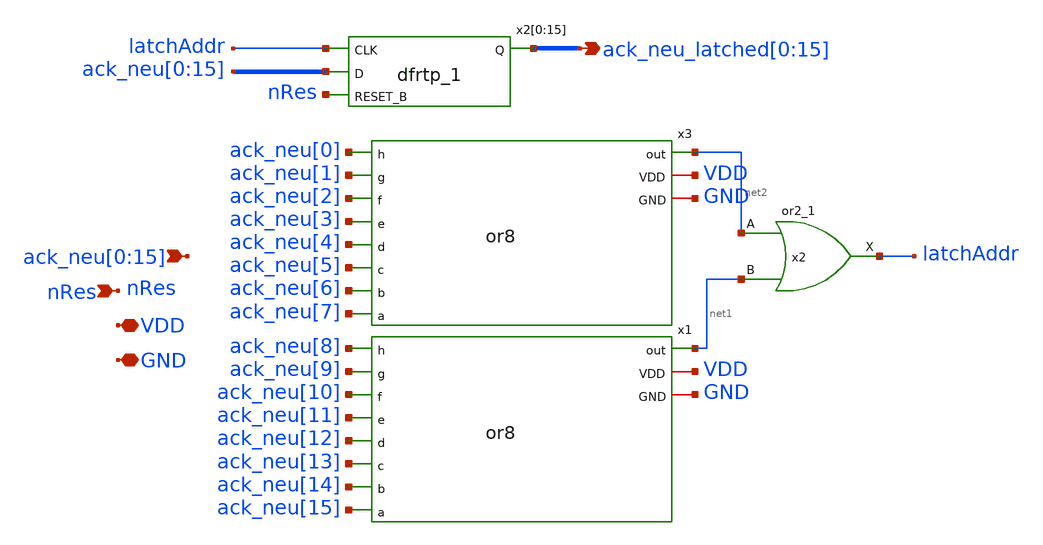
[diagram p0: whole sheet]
** sch_path: design/xschem/output_latch_16_neu.sch
**.subckt output_latch_16_neu
*+ ack_neu[0],ack_neu[1],ack_neu[2],ack_neu[3],ack_neu[4],ack_neu[5],ack_neu[6],ack_neu[7],ack_neu[8],ack_neu[9],ack_neu[10],ack_neu[11],ack_neu[12],ack_neu[13],ack_neu[14],ack_neu[15] nRes
*+ ack_neu_latched[0],ack_neu_latched[1],ack_neu_latched[2],ack_neu_latched[3],ack_neu_latched[4],ack_neu_latched[5],ack_neu_latched[6],ack_neu_latched[7],ack_neu_latched[8],ack_neu_latched[9],ack_neu_latched[10],ack_neu_latched[11],ack_neu_latched[12],ack_neu_latched[13],ack_neu_latched[14],ack_neu_latched[15] VDD GND
*.ipin
*+ ack_neu[0],ack_neu[1],ack_neu[2],ack_neu[3],ack_neu[4],ack_neu[5],ack_neu[6],ack_neu[7],ack_neu[8],ack_neu[9],ack_neu[10],ack_neu[11],ack_neu[12],ack_neu[13],ack_neu[14],ack_neu[15]
*.ipin nRes
*.opin
*+ ack_neu_latched[0],ack_neu_latched[1],ack_neu_latched[2],ack_neu_latched[3],ack_neu_latched[4],ack_neu_latched[5],ack_neu_latched[6],ack_neu_latched[7],ack_neu_latched[8],ack_neu_latched[9],ack_neu_latched[10],ack_neu_latched[11],ack_neu_latched[12],ack_neu_latched[13],ack_neu_latched[14],ack_neu_latched[15]
*.iopin VDD
*.iopin GND
x2[0] latchAddr ack_neu[0] nRes GND GND VDD VDD ack_neu_latched[0] sky130_fd_sc_hd__dfrtp_1
x2[1] latchAddr ack_neu[1] nRes GND GND VDD VDD ack_neu_latched[1] sky130_fd_sc_hd__dfrtp_1
x2[2] latchAddr ack_neu[2] nRes GND GND VDD VDD ack_neu_latched[2] sky130_fd_sc_hd__dfrtp_1
x2[3] latchAddr ack_neu[3] nRes GND GND VDD VDD ack_neu_latched[3] sky130_fd_sc_hd__dfrtp_1
x2[4] latchAddr ack_neu[4] nRes GND GND VDD VDD ack_neu_latched[4] sky130_fd_sc_hd__dfrtp_1
x2[5] latchAddr ack_neu[5] nRes GND GND VDD VDD ack_neu_latched[5] sky130_fd_sc_hd__dfrtp_1
x2[6] latchAddr ack_neu[6] nRes GND GND VDD VDD ack_neu_latched[6] sky130_fd_sc_hd__dfrtp_1
x2[7] latchAddr ack_neu[7] nRes GND GND VDD VDD ack_neu_latched[7] sky130_fd_sc_hd__dfrtp_1
x2[8] latchAddr ack_neu[8] nRes GND GND VDD VDD ack_neu_latched[8] sky130_fd_sc_hd__dfrtp_1
x2[9] latchAddr ack_neu[9] nRes GND GND VDD VDD ack_neu_latched[9] sky130_fd_sc_hd__dfrtp_1
x2[10] latchAddr ack_neu[10] nRes GND GND VDD VDD ack_neu_latched[10] sky130_fd_sc_hd__dfrtp_1
x2[11] latchAddr ack_neu[11] nRes GND GND VDD VDD ack_neu_latched[11] sky130_fd_sc_hd__dfrtp_1
x2[12] latchAddr ack_neu[12] nRes GND GND VDD VDD ack_neu_latched[12] sky130_fd_sc_hd__dfrtp_1
x2[13] latchAddr ack_neu[13] nRes GND GND VDD VDD ack_neu_latched[13] sky130_fd_sc_hd__dfrtp_1
x2[14] latchAddr ack_neu[14] nRes GND GND VDD VDD ack_neu_latched[14] sky130_fd_sc_hd__dfrtp_1
x2[15] latchAddr ack_neu[15] nRes GND GND VDD VDD ack_neu_latched[15] sky130_fd_sc_hd__dfrtp_1
x3 ack_neu[0] ack_neu[1] ack_neu[2] ack_neu[3] net2 ack_neu[4] ack_neu[5] ack_neu[6] ack_neu[7] VDD
+ GND or8
x1 ack_neu[8] ack_neu[9] ack_neu[10] ack_neu[11] net1 ack_neu[12] ack_neu[13] ack_neu[14]
+ ack_neu[15] VDD GND or8
x2 net2 net1 GND GND VDD VDD latchAddr sky130_fd_sc_hd__or2_1
**.ends

* expanding   symbol:  or8.sym # of pins=11
** sym_path: design/xschem/or8.sym
** sch_path: design/xschem/or8.sch
.subckt or8 h g f e out d c b a VDD GND
*.ipin a
*.ipin b
*.ipin c
*.ipin d
*.ipin e
*.ipin f
*.ipin g
*.ipin h
*.opin out
*.iopin VDD
*.iopin GND
x1 h g f e GND GND VDD VDD net1 sky130_fd_sc_hd__or4_1
x2 d c b a GND GND VDD VDD net2 sky130_fd_sc_hd__or4_1
x3 net1 net2 GND GND VDD VDD out sky130_fd_sc_hd__or2_1
.ends

.end
